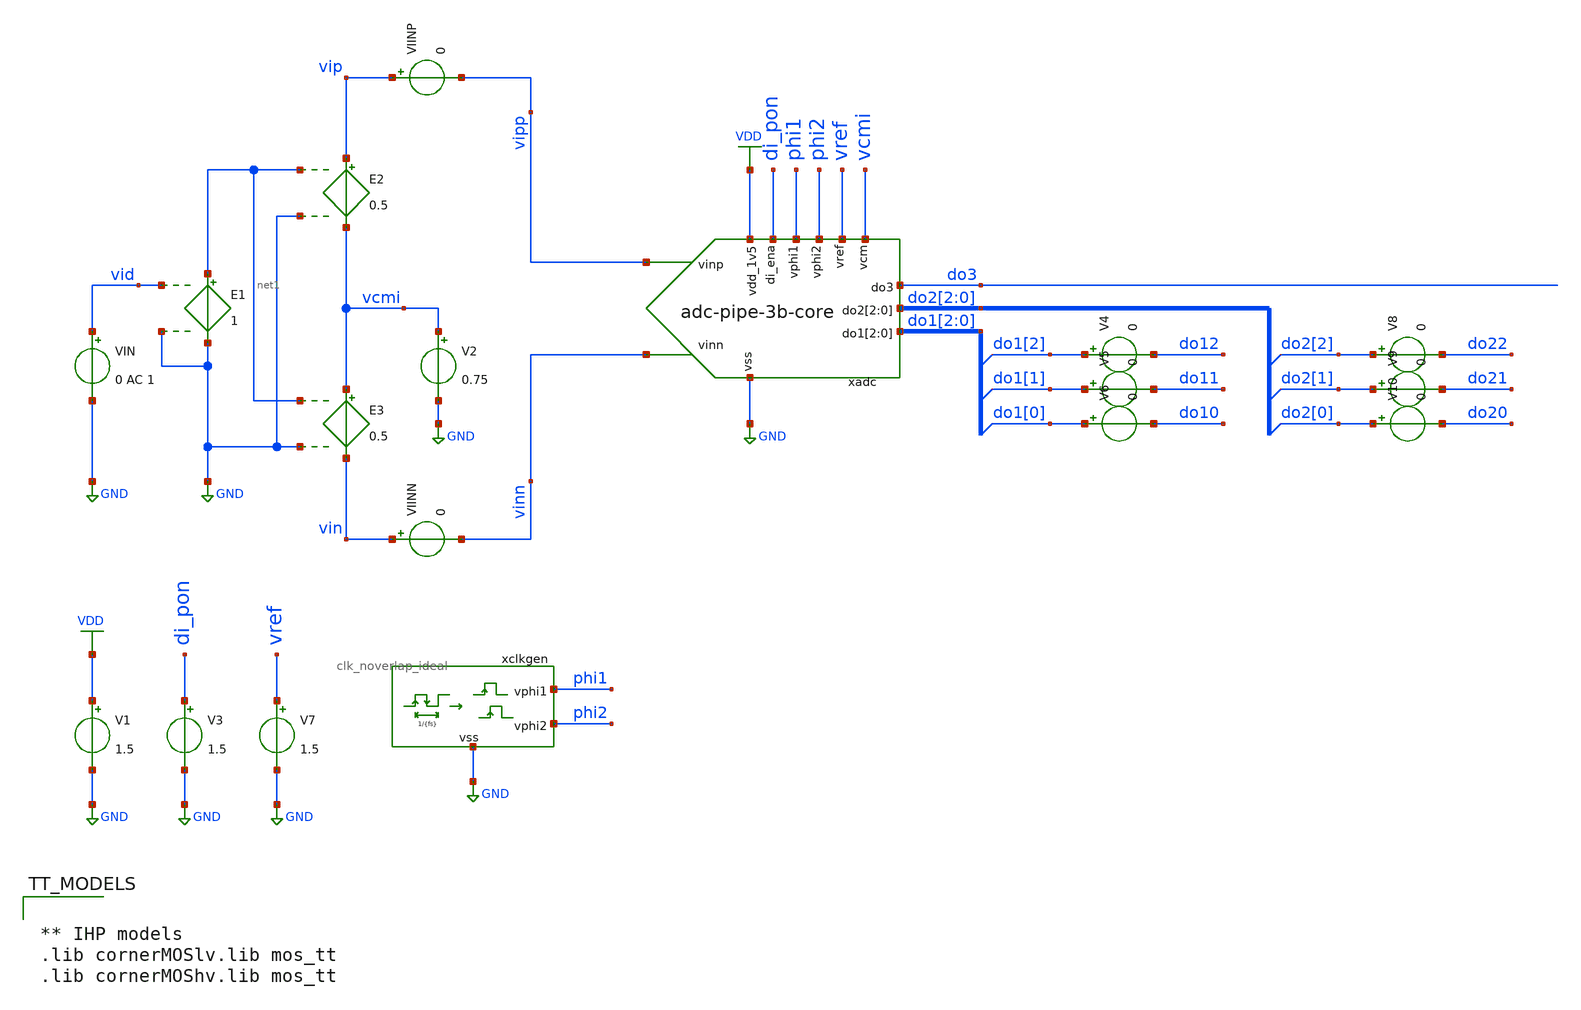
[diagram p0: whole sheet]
** sch_path: xschem/adc-pipe-3b-core_tb.sch
**.subckt adc-pipe-3b-core_tb
V1 VDD GND 1.5
V3 di_pon GND 1.5
V2 vcmi GND 0.75
E3 vcmi vin net1 GND 0.5
E2 vip vcmi net1 GND 0.5
VIN vid GND 0 AC 1
E1 net1 GND vid GND 1
VIINP vip vipp 0
VIINN vin vinn 0
xclkgen phi1 phi2 GND clk_noverlap_ideal fs={fs} tnover=50n tdelay=0 trf=5n
V7 vref GND 1.5
xadc di_pon phi2 phi1 vcmi vref VDD vipp vinn do3 do2[2] do2[1] do2[0] do1[2] do1[1] do1[0] GND
+ adc-pipe-3b-core
V4 do1[2] do12 0
V5 do1[1] do11 0
V6 do1[0] do10 0
V8 do2[2] do22 0
V9 do2[1] do21 0
V10 do2[0] do20 0
**** begin user architecture code


.include adc-pipe-3b-core_tb.save
.options savecurrents
.options method=gear reltol=1e-4
.options sparse
.param fs=2Meg
.param ibias=1.5u
.param cap=100f
.param cap_load = 100f
.param ron=1
.param roff=1G

.control
save vin vip vid vcmi phi1 phi2 vref do10 do11 do12 do20 do21 do22 do3
save xadc.vres1p xadc.vres1n xadc.vres2p xadc.vres2n
save xadc.xmdac1.vdac_p xadc.mdac1.vdac_n xadc.xmdac1.vgndp xadc.xmdac1.vgndn xadc.xmdac1.vfb
+ xadc.xmdac1.vbp
save xadc.xmdac1.xc1.vc_p xadc.xmdac1.xc2.vc_p xadc.xmdac1.xc3.vc_p xadc.xmdac1.xc4.vc_p
save xadc.xmdac2.vdac_p xadc.mdac2.vdac_n xadc.xmdac2.vgndp xadc.xmdac2.vgndn xadc.xmdac2.vfb
+ xadc.xmdac2.vbp
save xadc.xmdac2.xc1.vc_p xadc.xmdac2.xc2.vc_p xadc.xmdac2.xc3.vc_p xadc.xmdac2.xc4.vc_p

set wr_singlescale
set wr_vecnames
option numdgt=3

** Sim Options
set opSimOnly = 0

** Set sampling frequency
let fs = 2Meg

** Set Startup time
let n_per_startup = 100
let t_delay = n_per_startup/fs

** Set input signal
let f_sig = 100k
let tper_sig = 1/f_sig
let tfr_sig = tper_sig*5/10
let ton_sig = tper_sig*1/1000

** Set transient simulation parameters
let tstep = 0.001/fs
let tstop = 2/f_sig+t_delay
let tstart = t_delay

alter @VIN[DC] = 0.0

** Main Simulations
if $opSimOnly eq 0
	** Set sources
	*alter @VIN[PULSE]=[ -1.5 1.5 0 $&tfr_sig $&tfr_sig $&ton_sig $&tper_sig 0 ]
	alter @VIN[SIN] = [ 0 1 $&f_sig t_delay 0 0 ]
	tran $&tstep $&tstop $&tstart

	setplot tran1
	let vid = v(vid)
	let vres1 = xadc.vres1p - xadc.vres1n
	let vres2 = xadc.vres2p - xadc.vres2n

	let vcmo1 = (xadc.vres1p+xadc.vres1n)/2
	let vcmo2 = (xadc.vres2p+xadc.vres2n)/2
	let vcmi1 = (xadc.xmdac1.vgndp+xadc.xmdac1.vgndn)/2
	let vcmi2 = (xadc.xmdac2.vgndp+xadc.xmdac2.vgndn)/2

	let vcap_in_n = v(xadc.xmdac1.xc2.vc_p,xadc.xmdac1.vgndn)
	let v_in_n = v(vin,vcmi1)
	let v_dac_p = v(xadc.xmdac1.vdac_p,vcmi1)
	let vcap_in_p = v(xadc.xmdac1.xc4.vc_p,xadc.xmdac1.vgndp)
	let v_in_p = v(vip,vcmi)
	let v_dac_n = v(xadc.xmdac1.vdac_n,vcmi1)

	let err1 = 2*vid-vres1
	let err2 = 2*vres1-vres2

	plot vid vres1 vcmo1 vcmi1 phi2
	plot vcap_in_n v_in_n v_dac_p vcap_in_p v_in_p v_dac_n
	plot err1
	plot err2
	plot vid vres1 vres2
	plot do12 do11 do10 vid
	plot do22 do21 do20 vres1
	plot do3 vres2

end

alter @VIN[DC] = 0
optran 0 0 0 0.1u $&t_delay 0
op
remzerovec
write adc-pipe-3b-core_tb.raw
.endc



** IHP models
.lib cornerMOSlv.lib mos_tt
.lib cornerMOShv.lib mos_tt


**** end user architecture code
**.ends
.GLOBAL GND
.GLOBAL VDD
.end
